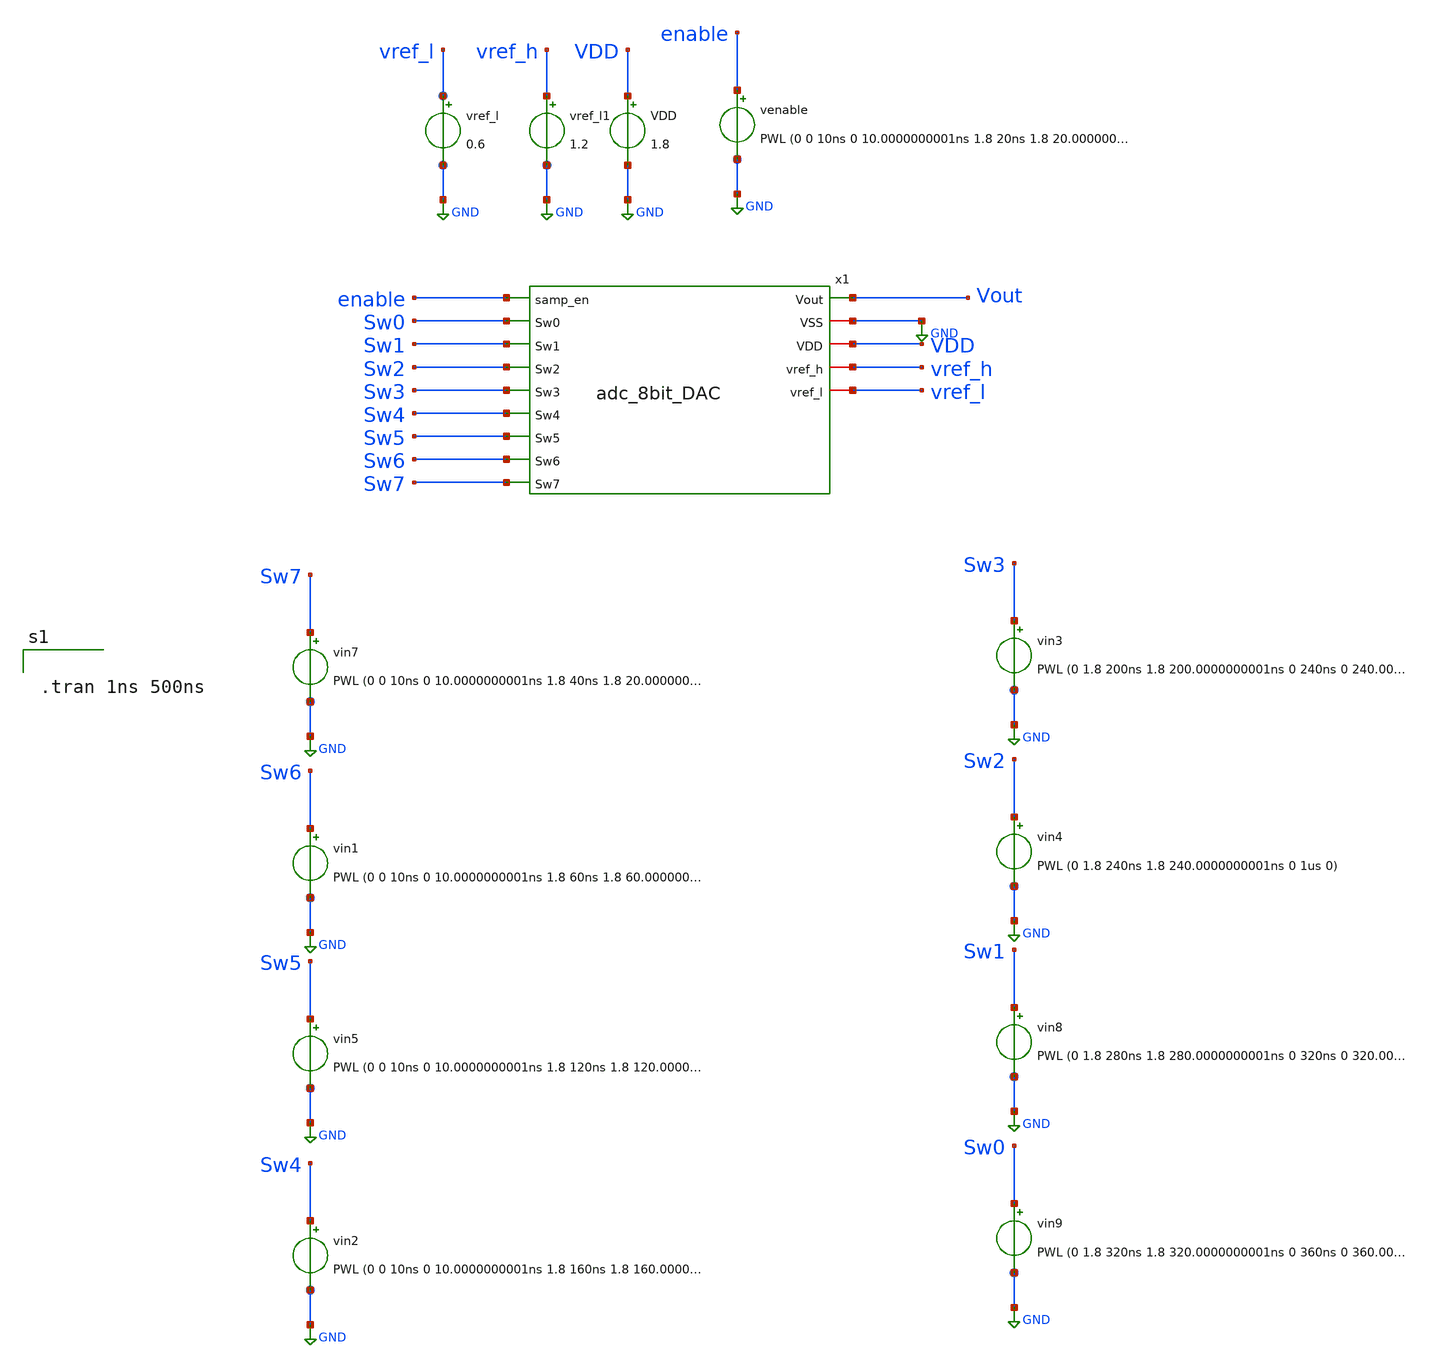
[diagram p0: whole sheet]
** sch_path: adc_8bit_DAC_tb.sch
**.subckt adc_8bit_DAC_tb
x1 Vout GND enable Sw0 VDD Sw1 vref_h Sw2 vref_l Sw3 Sw4 Sw5 Sw6 Sw7 adc_8bit_DAC
VDD VDD GND 1.8
vref_l1 vref_h GND 1.2
vin7 Sw7 GND PWL (0 0 10ns 0 10.0000000001ns 1.8 40ns 1.8 20.0000000000001ns 0 1us 0)
vin4 Sw2 GND PWL (0 1.8 240ns 1.8 240.0000000001ns 0 1us 0)
vin9 Sw0 GND PWL (0 1.8 320ns 1.8 320.0000000001ns 0 360ns 0 360.0000000000001ns 1.8 1us 1.8)
vin8 Sw1 GND PWL (0 1.8 280ns 1.8 280.0000000001ns 0 320ns 0 320.0000000000001ns 1.8 1us 1.8)
vin5 Sw5 GND PWL (0 0 10ns 0 10.0000000001ns 1.8 120ns 1.8 120.0000000000001ns 0 1us 0)
vin2 Sw4 GND PWL (0 0 10ns 0 10.0000000001ns 1.8 160ns 1.8 160.0000000000001ns 0 1us 0)
vin1 Sw6 GND PWL (0 0 10ns 0 10.0000000001ns 1.8 60ns 1.8 60.0000000000001ns 0 120ns 0 120.0001ns
+ 1.8 1us 1.8)
vin3 Sw3 GND PWL (0 1.8 200ns 1.8 200.0000000001ns 0 240ns 0 240.0000000000001ns 1.8 1us 1.8)
vref_l vref_l GND 0.6
venable enable GND PWL (0 0 10ns 0 10.0000000001ns 1.8 20ns 1.8 20.0000000000001ns 0 1us 0)
**** begin user architecture code


.tran 1ns 500ns


** opencircuitdesign pdks install
.lib $::SKYWATER_MODELS/sky130.lib.spice tt
.include $::SKYWATER_STDCELLS/sky130_fd_sc_hd.spice

**** end user architecture code
**.ends

* expanding   symbol:  adc_8bit_DAC.sym # of pins=14
** sym_path: adc_8bit_DAC.sym
** sch_path: adc_8bit_DAC.sch
.subckt adc_8bit_DAC Vout VSS samp_en Sw0 VDD Sw1 vref_h Sw2 vref_l Sw3 Sw4 Sw5 Sw6 Sw7
*.ipin Sw0
*.ipin samp_en
*.iopin VSS
*.iopin VDD
*.iopin vref_l
*.opin Vout
*.ipin Sw1
*.ipin Sw2
*.ipin Sw3
*.ipin Sw4
*.ipin Sw5
*.ipin Sw6
*.ipin Sw7
*.iopin vref_h
XM23 net8 Sw0 vref_l VSS sky130_fd_pr__nfet_01v8 L=0.24 W=2 nf=1 ad='int((nf+1)/2) * W/nf * 0.29' as='int((nf+2)/2) * W/nf * 0.29'
+ pd='2*int((nf+1)/2) * (W/nf + 0.29)' ps='2*int((nf+2)/2) * (W/nf + 0.29)' nrd='0.29 / W' nrs='0.29 / W'
+ sa=0 sb=0 sd=0 mult=1 m=1
XM21 net6 Sw2 vref_l VSS sky130_fd_pr__nfet_01v8 L=0.24 W=1 nf=1 ad='int((nf+1)/2) * W/nf * 0.29' as='int((nf+2)/2) * W/nf * 0.29'
+ pd='2*int((nf+1)/2) * (W/nf + 0.29)' ps='2*int((nf+2)/2) * (W/nf + 0.29)' nrd='0.29 / W' nrs='0.29 / W'
+ sa=0 sb=0 sd=0 mult=1 m=1
XM24 net7 Sw1 vref_l VSS sky130_fd_pr__nfet_01v8 L=0.24 W=1 nf=1 ad='int((nf+1)/2) * W/nf * 0.29' as='int((nf+2)/2) * W/nf * 0.29'
+ pd='2*int((nf+1)/2) * (W/nf + 0.29)' ps='2*int((nf+2)/2) * (W/nf + 0.29)' nrd='0.29 / W' nrs='0.29 / W'
+ sa=0 sb=0 sd=0 mult=1 m=1
XM25 net5 Sw3 vref_l VSS sky130_fd_pr__nfet_01v8 L=0.24 W=1 nf=1 ad='int((nf+1)/2) * W/nf * 0.29' as='int((nf+2)/2) * W/nf * 0.29'
+ pd='2*int((nf+1)/2) * (W/nf + 0.29)' ps='2*int((nf+2)/2) * (W/nf + 0.29)' nrd='0.29 / W' nrs='0.29 / W'
+ sa=0 sb=0 sd=0 mult=1 m=1
XM26 Vout samp_en vref_l VSS sky130_fd_pr__nfet_01v8 L=0.3 W=10 nf=1 ad='int((nf+1)/2) * W/nf * 0.29'
+ as='int((nf+2)/2) * W/nf * 0.29' pd='2*int((nf+1)/2) * (W/nf + 0.29)' ps='2*int((nf+2)/2) * (W/nf + 0.29)'
+ nrd='0.29 / W' nrs='0.29 / W' sa=0 sb=0 sd=0 mult=1 m=1
XM27 net1 Sw4 vref_l VSS sky130_fd_pr__nfet_01v8 L=0.24 W=1 nf=1 ad='int((nf+1)/2) * W/nf * 0.29' as='int((nf+2)/2) * W/nf * 0.29'
+ pd='2*int((nf+1)/2) * (W/nf + 0.29)' ps='2*int((nf+2)/2) * (W/nf + 0.29)' nrd='0.29 / W' nrs='0.29 / W'
+ sa=0 sb=0 sd=0 mult=1 m=1
XM28 net2 Sw5 vref_l VSS sky130_fd_pr__nfet_01v8 L=0.24 W=2 nf=1 ad='int((nf+1)/2) * W/nf * 0.29' as='int((nf+2)/2) * W/nf * 0.29'
+ pd='2*int((nf+1)/2) * (W/nf + 0.29)' ps='2*int((nf+2)/2) * (W/nf + 0.29)' nrd='0.29 / W' nrs='0.29 / W'
+ sa=0 sb=0 sd=0 mult=1 m=1
XM29 net3 Sw6 vref_l VSS sky130_fd_pr__nfet_01v8 L=0.24 W=2 nf=1 ad='int((nf+1)/2) * W/nf * 0.29' as='int((nf+2)/2) * W/nf * 0.29'
+ pd='2*int((nf+1)/2) * (W/nf + 0.29)' ps='2*int((nf+2)/2) * (W/nf + 0.29)' nrd='0.29 / W' nrs='0.29 / W'
+ sa=0 sb=0 sd=0 mult=1 m=1
XM30 net4 Sw7 vref_l VSS sky130_fd_pr__nfet_01v8 L=0.24 W=2 nf=1 ad='int((nf+1)/2) * W/nf * 0.29' as='int((nf+2)/2) * W/nf * 0.29'
+ pd='2*int((nf+1)/2) * (W/nf + 0.29)' ps='2*int((nf+2)/2) * (W/nf + 0.29)' nrd='0.29 / W' nrs='0.29 / W'
+ sa=0 sb=0 sd=0 mult=1 m=1
XM9 vref_h Sw0 net8 VDD sky130_fd_pr__pfet_01v8 L=0.24 W=2 nf=1 ad='int((nf+1)/2) * W/nf * 0.29' as='int((nf+2)/2) * W/nf * 0.29'
+ pd='2*int((nf+1)/2) * (W/nf + 0.29)' ps='2*int((nf+2)/2) * (W/nf + 0.29)' nrd='0.29 / W' nrs='0.29 / W'
+ sa=0 sb=0 sd=0 mult=1 m=1
XM1 vref_h Sw1 net7 VDD sky130_fd_pr__pfet_01v8 L=0.24 W=1 nf=1 ad='int((nf+1)/2) * W/nf * 0.29' as='int((nf+2)/2) * W/nf * 0.29'
+ pd='2*int((nf+1)/2) * (W/nf + 0.29)' ps='2*int((nf+2)/2) * (W/nf + 0.29)' nrd='0.29 / W' nrs='0.29 / W'
+ sa=0 sb=0 sd=0 mult=1 m=1
XM2 vref_h Sw2 net6 VDD sky130_fd_pr__pfet_01v8 L=0.24 W=1 nf=1 ad='int((nf+1)/2) * W/nf * 0.29' as='int((nf+2)/2) * W/nf * 0.29'
+ pd='2*int((nf+1)/2) * (W/nf + 0.29)' ps='2*int((nf+2)/2) * (W/nf + 0.29)' nrd='0.29 / W' nrs='0.29 / W'
+ sa=0 sb=0 sd=0 mult=1 m=1
XM3 vref_h Sw3 net5 VDD sky130_fd_pr__pfet_01v8 L=0.24 W=1 nf=1 ad='int((nf+1)/2) * W/nf * 0.29' as='int((nf+2)/2) * W/nf * 0.29'
+ pd='2*int((nf+1)/2) * (W/nf + 0.29)' ps='2*int((nf+2)/2) * (W/nf + 0.29)' nrd='0.29 / W' nrs='0.29 / W'
+ sa=0 sb=0 sd=0 mult=1 m=1
XM4 vref_h Sw4 net1 VDD sky130_fd_pr__pfet_01v8 L=0.24 W=1 nf=1 ad='int((nf+1)/2) * W/nf * 0.29' as='int((nf+2)/2) * W/nf * 0.29'
+ pd='2*int((nf+1)/2) * (W/nf + 0.29)' ps='2*int((nf+2)/2) * (W/nf + 0.29)' nrd='0.29 / W' nrs='0.29 / W'
+ sa=0 sb=0 sd=0 mult=1 m=1
XM5 vref_h Sw5 net2 VDD sky130_fd_pr__pfet_01v8 L=0.24 W=2 nf=1 ad='int((nf+1)/2) * W/nf * 0.29' as='int((nf+2)/2) * W/nf * 0.29'
+ pd='2*int((nf+1)/2) * (W/nf + 0.29)' ps='2*int((nf+2)/2) * (W/nf + 0.29)' nrd='0.29 / W' nrs='0.29 / W'
+ sa=0 sb=0 sd=0 mult=1 m=1
XM6 vref_h Sw6 net3 VDD sky130_fd_pr__pfet_01v8 L=0.24 W=2 nf=1 ad='int((nf+1)/2) * W/nf * 0.29' as='int((nf+2)/2) * W/nf * 0.29'
+ pd='2*int((nf+1)/2) * (W/nf + 0.29)' ps='2*int((nf+2)/2) * (W/nf + 0.29)' nrd='0.29 / W' nrs='0.29 / W'
+ sa=0 sb=0 sd=0 mult=1 m=1
XM7 vref_h Sw7 net4 VDD sky130_fd_pr__pfet_01v8 L=0.24 W=2 nf=1 ad='int((nf+1)/2) * W/nf * 0.29' as='int((nf+2)/2) * W/nf * 0.29'
+ pd='2*int((nf+1)/2) * (W/nf + 0.29)' ps='2*int((nf+2)/2) * (W/nf + 0.29)' nrd='0.29 / W' nrs='0.29 / W'
+ sa=0 sb=0 sd=0 mult=1 m=1
XC3 Vout net7 sky130_fd_pr__cap_mim_m3_1 W=1 L=1 MF=1 m=1
XC4 Vout net6 sky130_fd_pr__cap_mim_m3_1 W=2 L=1.1 MF=1 m=1
XC5 Vout net5 sky130_fd_pr__cap_mim_m3_1 W=4 L=1.2 MF=1 m=1
XC6 Vout net1 sky130_fd_pr__cap_mim_m3_1 W=8 L=1.2 MF=1 m=1
XC2 Vout net9 sky130_fd_pr__cap_mim_m3_1 W=1 L=1 MF=1 m=1
XC10 Vout vref_l sky130_fd_pr__cap_mim_m3_1 W=1 L=1 MF=1 m=1
XC11 net9 net8 sky130_fd_pr__cap_mim_m3_1 W=1 L=1 MF=1 m=1
XC1 Vout net2 sky130_fd_pr__cap_mim_m3_1 W=8 L=1.2 MF=1 m=1
XC7 Vout net2 sky130_fd_pr__cap_mim_m3_1 W=8 L=1.2 MF=1 m=1
XC8 Vout net3 sky130_fd_pr__cap_mim_m3_1 W=8 L=1.2 MF=1 m=1
XC12 Vout net3 sky130_fd_pr__cap_mim_m3_1 W=8 L=1.2 MF=1 m=1
XC13 Vout net3 sky130_fd_pr__cap_mim_m3_1 W=8 L=1.2 MF=1 m=1
XC14 Vout net3 sky130_fd_pr__cap_mim_m3_1 W=8 L=1.2 MF=1 m=1
XC9 Vout net4 sky130_fd_pr__cap_mim_m3_1 W=8 L=1.2 MF=1 m=1
XC15 Vout net4 sky130_fd_pr__cap_mim_m3_1 W=8 L=1.2 MF=1 m=1
XC16 Vout net4 sky130_fd_pr__cap_mim_m3_1 W=8 L=1.2 MF=1 m=1
XC17 Vout net4 sky130_fd_pr__cap_mim_m3_1 W=8 L=1.2 MF=1 m=1
XC18 Vout net4 sky130_fd_pr__cap_mim_m3_1 W=8 L=1.2 MF=1 m=1
XC19 Vout net4 sky130_fd_pr__cap_mim_m3_1 W=8 L=1.2 MF=1 m=1
XC20 Vout net4 sky130_fd_pr__cap_mim_m3_1 W=8 L=1.2 MF=1 m=1
XC21 Vout net4 sky130_fd_pr__cap_mim_m3_1 W=8 L=1.2 MF=1 m=1
.ends

.GLOBAL GND
.end
